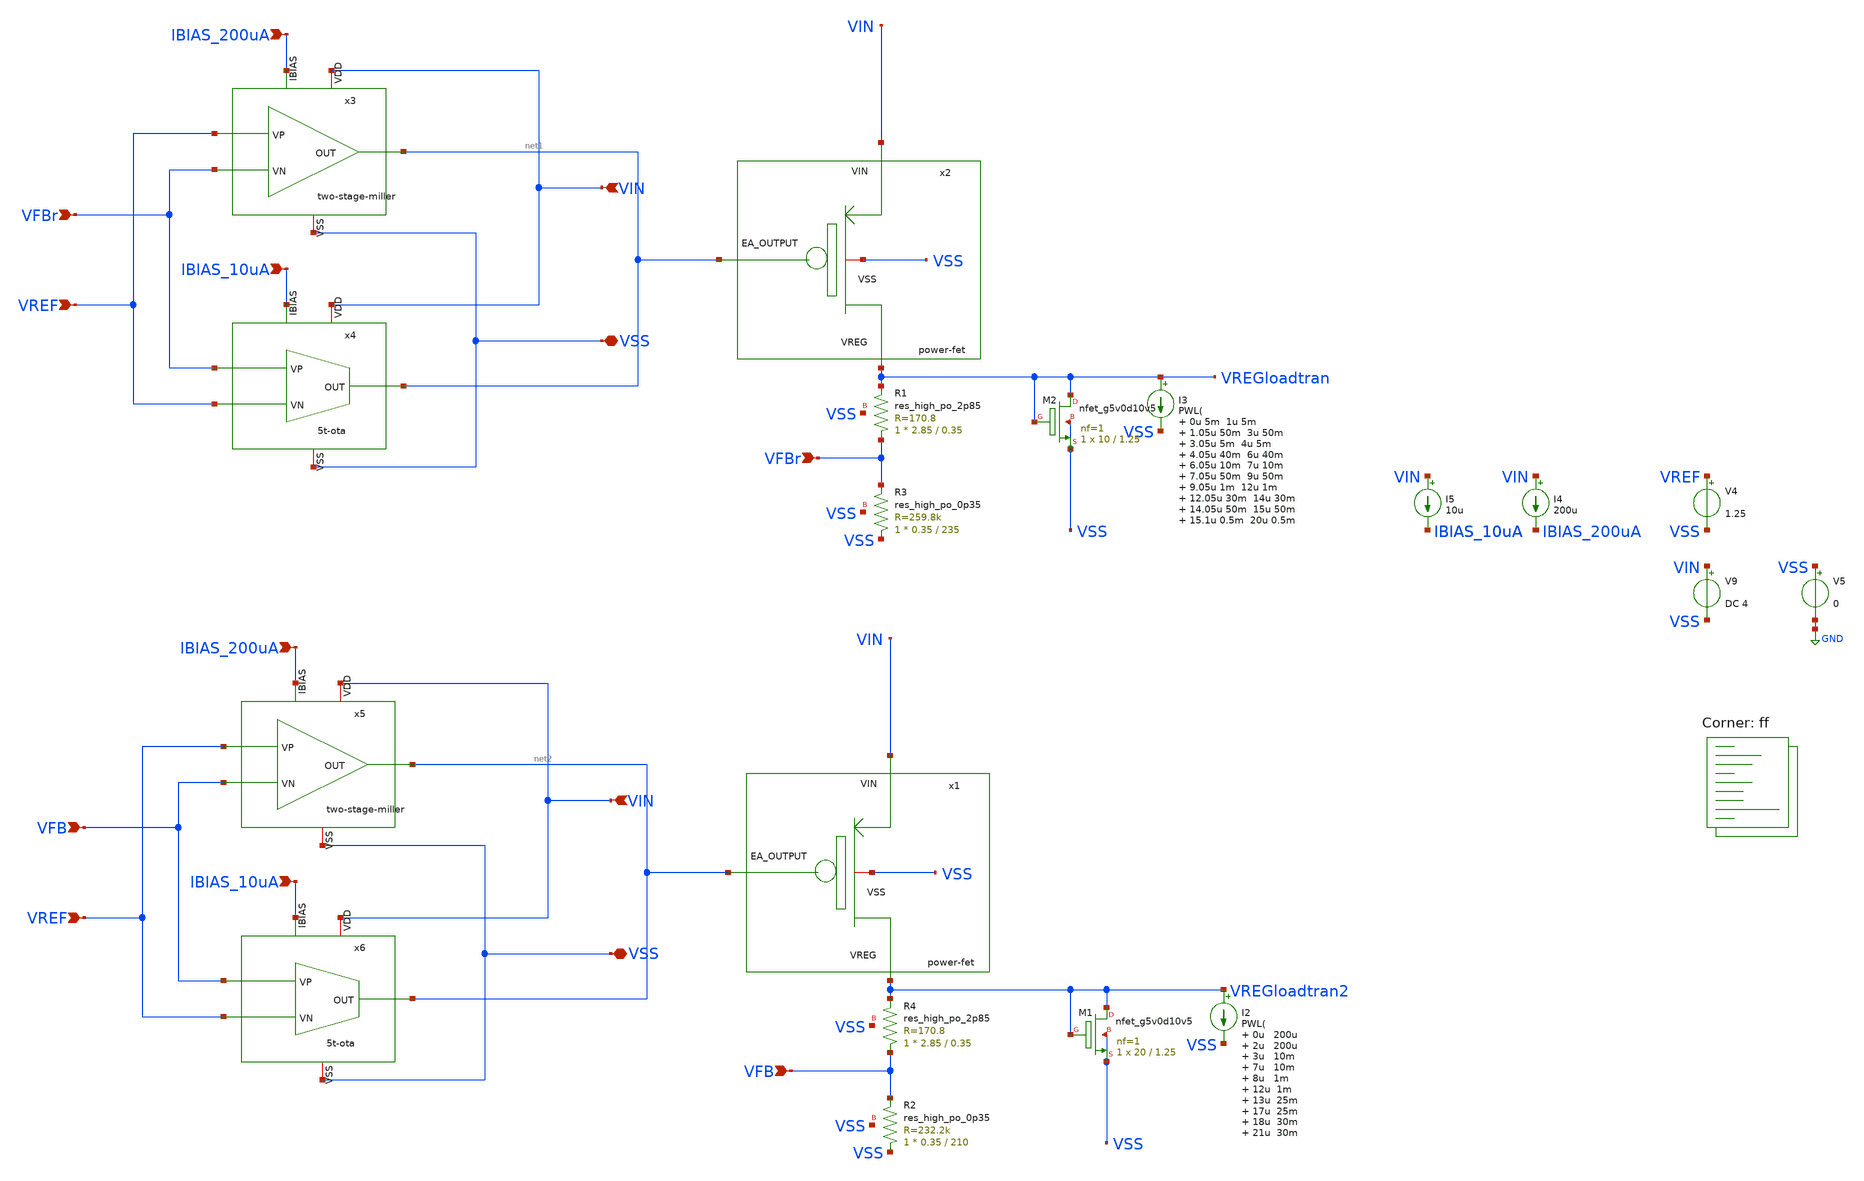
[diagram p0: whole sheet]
** sch_path: xschem/ldo-core/tb_tran_standalone.sch
**.subckt tb_tran_standalone VFBr VFBr VREF IBIAS_10uA IBIAS_200uA VIN VSS VFB VREF IBIAS_10uA
*+ IBIAS_200uA VIN VSS VFB
*.ipin VFBr
*.ipin VFBr
*.ipin VREF
*.ipin IBIAS_10uA
*.ipin IBIAS_200uA
*.ipin VIN
*.iopin VSS
*.ipin VFB
*.ipin VREF
*.ipin IBIAS_10uA
*.ipin IBIAS_200uA
*.ipin VIN
*.iopin VSS
*.ipin VFB
x2 VIN VSS net1 VREGloadtran power-fet
XR3 VSS VFBr VSS sky130_fd_pr__res_high_po_0p35 L=235 mult=1 m=1
XR1 VFBr VREGloadtran VSS sky130_fd_pr__res_high_po_2p85 L=0.35 mult=1 m=1
x3 VIN net1 VREF VFBr IBIAS_200uA VSS two-stage-miller
x4 VIN net1 IBIAS_10uA VREF VFBr VSS 5t-ota
I4 VIN IBIAS_200uA 200u
x1 VIN VSS net2 VREGloadtran2 power-fet
XR4 VFB VREGloadtran2 VSS sky130_fd_pr__res_high_po_2p85 L=0.35 mult=1 m=1
x5 VIN net2 VREF VFB IBIAS_200uA VSS two-stage-miller
x6 VIN net2 IBIAS_10uA VREF VFB VSS 5t-ota
I3 VREGloadtran VSS PWL( 0u 5m 1u 5m 1.05u 50m 3u 50m 3.05u 5m 4u 5m 4.05u 40m 6u 40m 6.05u 10m 7u
+ 10m 7.05u 50m 9u 50m 9.05u 1m 12u 1m 12.05u 30m 14u 30m 14.05u 50m 15u 50m 15.1u 0.5m 20u 0.5m
)
XR2 VSS VFB VSS sky130_fd_pr__res_high_po_0p35 L=210 mult=1 m=1
I2 VREGloadtran2 VSS PWL( 0u 200u 2u 200u 3u 10m 7u 10m 8u 1m 12u 1m 13u 25m 17u 25m 18u 30m 21u 30m
+ 22u 15m 24u 15m 24.5u 0.5m 25u 0.5m
)
V4 VREF VSS 1.25
V5 VSS GND 0
V9 VIN VSS DC 4
I5 VIN IBIAS_10uA 10u
XM2 VREGloadtran VREGloadtran VSS VSS sky130_fd_pr__nfet_g5v0d10v5 L=1.25 W=10 nf=1 ad='int((nf+1)/2) * W/nf * 0.29'
+ as='int((nf+2)/2) * W/nf * 0.29' pd='2*int((nf+1)/2) * (W/nf + 0.29)' ps='2*int((nf+2)/2) * (W/nf + 0.29)'
+ nrd='0.29 / W' nrs='0.29 / W' sa=0 sb=0 sd=0 mult=1 m=1
XM1 VREGloadtran2 VREGloadtran2 VSS VSS sky130_fd_pr__nfet_g5v0d10v5 L=1.25 W=20 nf=1 ad='int((nf+1)/2) * W/nf * 0.29'
+ as='int((nf+2)/2) * W/nf * 0.29' pd='2*int((nf+1)/2) * (W/nf + 0.29)' ps='2*int((nf+2)/2) * (W/nf + 0.29)'
+ nrd='0.29 / W' nrs='0.29 / W' sa=0 sb=0 sd=0 mult=1 m=1
**** begin user architecture code



.temp 27
.control

tran 0.1u 30u

* Nominal output voltage (from regulation region)
let Vout_nom = 1.25
let Vout_95  = 0.95*Vout_nom

* Find Vin where Vout crosses 95%
meas dc Vin_do find v(vin) when v(vreg)=Vout_95

* Measure Vout at that Vin (for completeness)
meas dc Vout_do find v(vreg) when v(vreg)=Vout_95

* Compute dropout voltage
let Vdo = Vin_do - Vout_do

* Compute overshoot, undershoot and peak-to-peak voltage
meas tran Vout_max MAX v(VREGloadtran)
meas tran Vout_min MIN v(VREGloadtran)
let vpp = Vout_max - Vout_min

print Vin_do Vout_do Vdo
print Vout_max Vout_min Vpp
plot VREGloadtran
plot VREGloadtran2
plot VREG
plot VIN
plot I(Vmeas)

.endc


.lib $::SKYWATER_MODELS/sky130.lib.spice ff
**** end user architecture code
**.ends
.GLOBAL GND
.end
